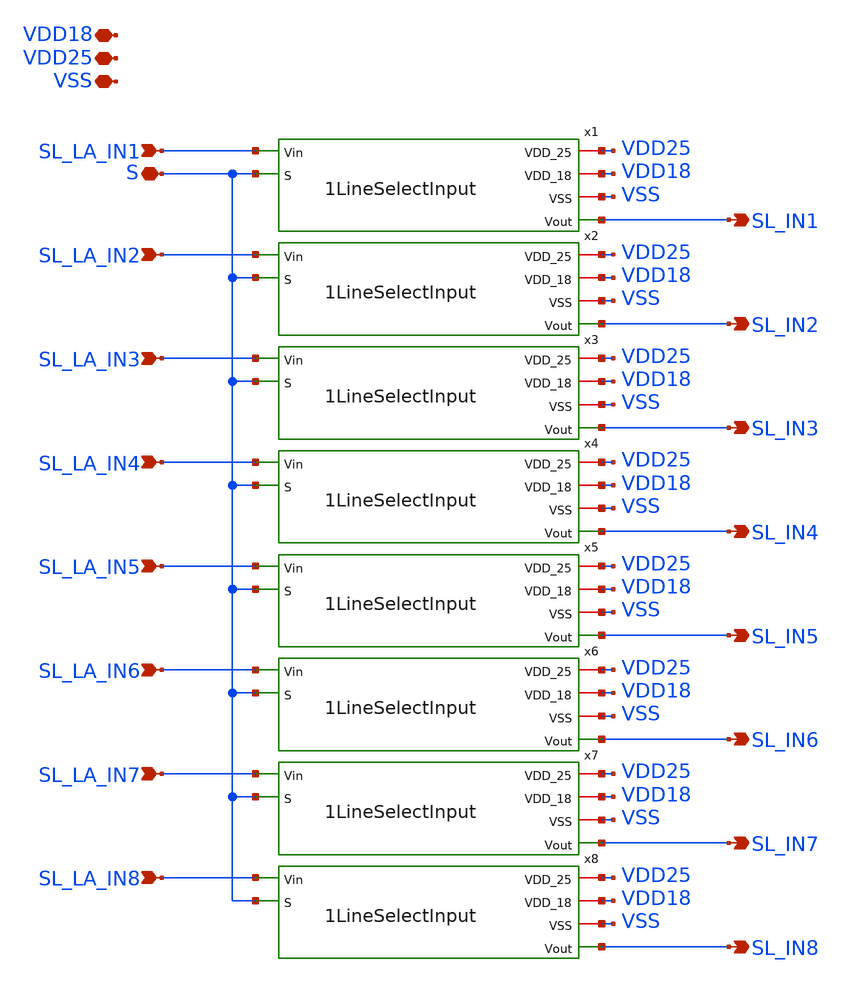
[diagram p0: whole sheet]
** sch_path: xschem/8LineSelectInput.sch
**.subckt 8LineSelectInput VDD25 VSS SL_LA_IN8 SL_LA_IN7 SL_LA_IN6 SL_LA_IN5 SL_LA_IN4 SL_LA_IN3
*+ SL_LA_IN2 SL_LA_IN1 S SL_IN8 SL_IN7 SL_IN6 SL_IN5 SL_IN4 SL_IN3 SL_IN2 SL_IN1 VDD18
*.iopin VDD25
*.iopin VSS
*.ipin SL_LA_IN8
*.ipin SL_LA_IN7
*.ipin SL_LA_IN6
*.ipin SL_LA_IN5
*.ipin SL_LA_IN4
*.ipin SL_LA_IN3
*.ipin SL_LA_IN2
*.ipin SL_LA_IN1
*.iopin S
*.opin SL_IN8
*.opin SL_IN7
*.opin SL_IN6
*.opin SL_IN5
*.opin SL_IN4
*.opin SL_IN3
*.opin SL_IN2
*.opin SL_IN1
*.iopin VDD18
x1 VDD25 VDD18 VSS SL_LA_IN1 SL_IN1 S 1LineSelectInput
x2 VDD25 VDD18 VSS SL_LA_IN2 SL_IN2 S 1LineSelectInput
x3 VDD25 VDD18 VSS SL_LA_IN3 SL_IN3 S 1LineSelectInput
x4 VDD25 VDD18 VSS SL_LA_IN4 SL_IN4 S 1LineSelectInput
x5 VDD25 VDD18 VSS SL_LA_IN5 SL_IN5 S 1LineSelectInput
x6 VDD25 VDD18 VSS SL_LA_IN6 SL_IN6 S 1LineSelectInput
x7 VDD25 VDD18 VSS SL_LA_IN7 SL_IN7 S 1LineSelectInput
x8 VDD25 VDD18 VSS SL_LA_IN8 SL_IN8 S 1LineSelectInput
**.ends

* expanding   symbol:  1LineSelectInput.sym # of pins=6
** sym_path: xschem/1LineSelectInput.sym
** sch_path: xschem/1LineSelectInput.sch
.subckt 1LineSelectInput VDD_25 VDD_18 VSS Vin Vout S
*.iopin VDD_18
*.iopin VSS
*.ipin Vin
*.opin Vout
*.ipin S
*.iopin VDD_25
x1 VDD_25 Vin Bout VSS Buffer
x2 SP VDD_18 Vout Bout VSS S TransmissionGate
x3 VDD_18 S SP VSS Inverter
.ends


* expanding   symbol:  Buffer.sym # of pins=4
** sym_path: xschem/Buffer.sym
** sch_path: xschem/Buffer.sch
.subckt Buffer VDD Vin Vout VSS
*.iopin VDD
*.iopin VSS
*.ipin Vin
*.opin Vout
x1 VDD Vin net1 VSS Inverter
x2 VDD net1 Vout VSS Inverter
.ends


* expanding   symbol:  TransmissionGate.sym # of pins=6
** sym_path: xschem/TransmissionGate.sym
** sch_path: xschem/TransmissionGate.sch
.subckt TransmissionGate SP VDD Out In VSS SN
*.opin Out
*.ipin In
*.ipin SP
*.iopin VDD
*.iopin VSS
*.ipin SN
XM1 In SN Out VSS sky130_fd_pr__nfet_g5v0d10v5 L=0.5 W=0.75 nf=1 ad='int((nf+1)/2) * W/nf * 0.29' as='int((nf+2)/2) * W/nf * 0.29'
+ pd='2*int((nf+1)/2) * (W/nf + 0.29)' ps='2*int((nf+2)/2) * (W/nf + 0.29)' nrd='0.29 / W' nrs='0.29 / W'
+ sa=0 sb=0 sd=0 mult=1 m=1
XM2 In SP Out VDD sky130_fd_pr__pfet_g5v0d10v5 L=0.5 W=1.5 nf=1 ad='int((nf+1)/2) * W/nf * 0.29' as='int((nf+2)/2) * W/nf * 0.29'
+ pd='2*int((nf+1)/2) * (W/nf + 0.29)' ps='2*int((nf+2)/2) * (W/nf + 0.29)' nrd='0.29 / W' nrs='0.29 / W'
+ sa=0 sb=0 sd=0 mult=1 m=1
.ends


* expanding   symbol:  Inverter.sym # of pins=4
** sym_path: xschem/Inverter.sym
** sch_path: xschem/Inverter.sch
.subckt Inverter VDD Vin Vout VSS
*.ipin Vin
*.iopin VDD
*.iopin VSS
*.opin Vout
XM1 Vout Vin VSS VSS sky130_fd_pr__nfet_g5v0d10v5 L=0.5 W=0.75 nf=1 ad='int((nf+1)/2) * W/nf * 0.29'
+ as='int((nf+2)/2) * W/nf * 0.29' pd='2*int((nf+1)/2) * (W/nf + 0.29)' ps='2*int((nf+2)/2) * (W/nf + 0.29)'
+ nrd='0.29 / W' nrs='0.29 / W' sa=0 sb=0 sd=0 mult=1 m=1
XM2 Vout Vin VDD VDD sky130_fd_pr__pfet_g5v0d10v5 L=0.5 W=1.5 nf=1 ad='int((nf+1)/2) * W/nf * 0.29' as='int((nf+2)/2) * W/nf * 0.29'
+ pd='2*int((nf+1)/2) * (W/nf + 0.29)' ps='2*int((nf+2)/2) * (W/nf + 0.29)' nrd='0.29 / W' nrs='0.29 / W'
+ sa=0 sb=0 sd=0 mult=1 m=1
.ends

.end
